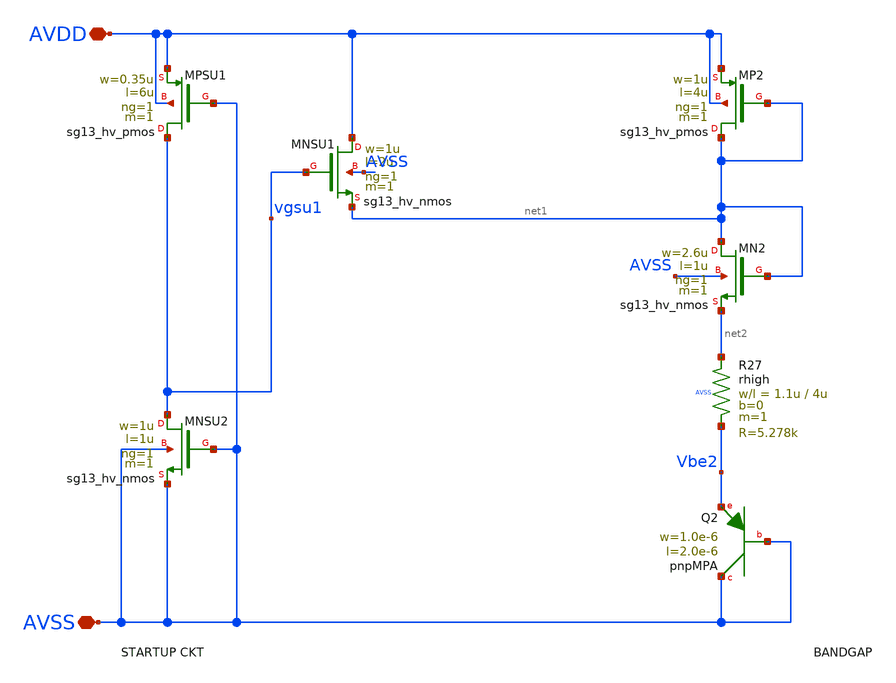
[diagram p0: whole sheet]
** sch_path: magic/sg13cmos5l_srout_tinybgr4magic.sch
**.subckt sg13cmos5l_srout_tinybgr4magic AVDD AVSS
*.iopin AVDD
*.iopin AVSS
XQ2 AVSS AVSS Vbe2 pnpMPA a=2p p=6u m=1
XMN2 net1 net1 net2 AVSS sg13_hv_nmos w=2.6u l=1u ng=1 m=1 mm_ok=1
XMP2 net1 net1 AVDD AVDD sg13_hv_pmos w=1u l=4u ng=1 m=1 mm_ok=1
XMNSU1 AVDD vgsu1 net1 AVSS sg13_hv_nmos w=1u l=2u ng=1 m=1 mm_ok=1
XMPSU1 vgsu1 AVSS AVDD AVDD sg13_hv_pmos w=0.35u l=6u ng=1 m=1 mm_ok=1
XMNSU2 vgsu1 AVSS AVSS AVSS sg13_hv_nmos w=1u l=1u ng=1 m=1 mm_ok=1
XR27 net2 Vbe2 AVSS rhigh w=1.1u l=4u m=1 b=0 mm_ok=1
**.ends
.end
